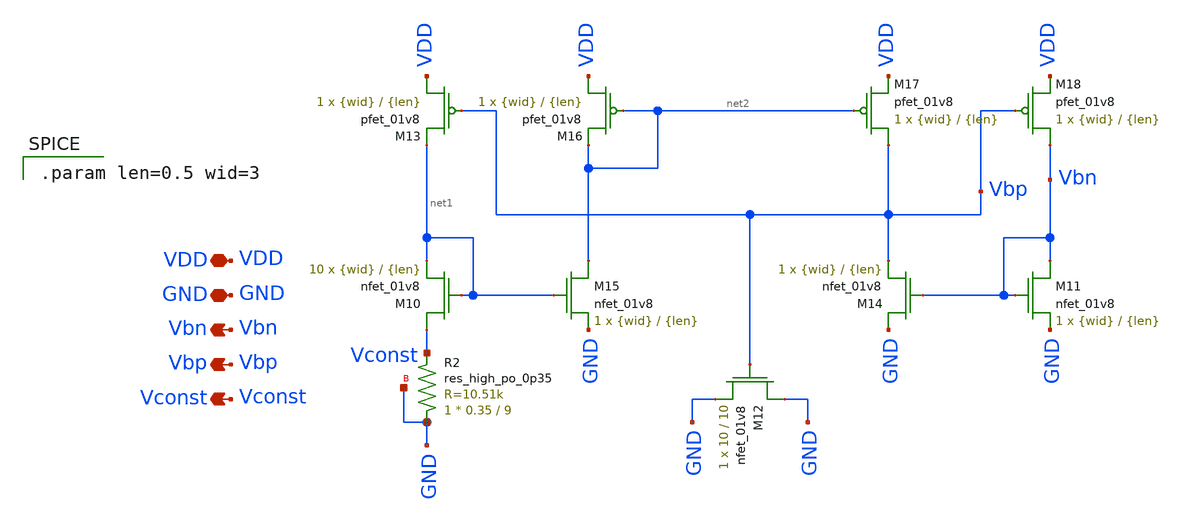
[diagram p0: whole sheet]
** sch_path: final/schematics/bias_gen/bias_gen.sch
**.subckt bias_gen VDD Vbp GND Vbn Vconst
*.iopin VDD
*.opin Vbp
*.iopin GND
*.opin Vbn
*.opin Vconst
XM10 Vconst net1 net1 GND sky130_fd_pr__nfet_01v8 L={len} W={wid} nf=1 ad='int((nf+1)/2) * W/nf * 0.29'
+ as='int((nf+2)/2) * W/nf * 0.29' pd='2*int((nf+1)/2) * (W/nf + 0.29)' ps='2*int((nf+2)/2) * (W/nf + 0.29)'
+ nrd='0.29 / W' nrs='0.29 / W' sa=0 sb=0 sd=0 mult=10 m=10
XM11 Vbn Vbn GND GND sky130_fd_pr__nfet_01v8 L={len} W={wid} nf=1 ad='int((nf+1)/2) * W/nf * 0.29' as='int((nf+2)/2) * W/nf * 0.29'
+ pd='2*int((nf+1)/2) * (W/nf + 0.29)' ps='2*int((nf+2)/2) * (W/nf + 0.29)' nrd='0.29 / W' nrs='0.29 / W'
+ sa=0 sb=0 sd=0 mult=1 m=1
XM12 GND Vbp GND GND sky130_fd_pr__nfet_01v8 L=10 W=10 nf=1 ad='int((nf+1)/2) * W/nf * 0.29' as='int((nf+2)/2) * W/nf * 0.29'
+ pd='2*int((nf+1)/2) * (W/nf + 0.29)' ps='2*int((nf+2)/2) * (W/nf + 0.29)' nrd='0.29 / W' nrs='0.29 / W'
+ sa=0 sb=0 sd=0 mult=1 m=1
XM13 VDD Vbp net1 VDD sky130_fd_pr__pfet_01v8 L={len} W={wid} nf=1 ad='int((nf+1)/2) * W/nf * 0.29' as='int((nf+2)/2) * W/nf * 0.29'
+ pd='2*int((nf+1)/2) * (W/nf + 0.29)' ps='2*int((nf+2)/2) * (W/nf + 0.29)' nrd='0.29 / W' nrs='0.29 / W'
+ sa=0 sb=0 sd=0 mult=1 m=1
XM14 GND Vbn Vbp GND sky130_fd_pr__nfet_01v8 L={len} W={wid} nf=1 ad='int((nf+1)/2) * W/nf * 0.29' as='int((nf+2)/2) * W/nf * 0.29'
+ pd='2*int((nf+1)/2) * (W/nf + 0.29)' ps='2*int((nf+2)/2) * (W/nf + 0.29)' nrd='0.29 / W' nrs='0.29 / W'
+ sa=0 sb=0 sd=0 mult=1 m=1
XM15 net2 net1 GND GND sky130_fd_pr__nfet_01v8 L={len} W={wid} nf=1 ad='int((nf+1)/2) * W/nf * 0.29'
+ as='int((nf+2)/2) * W/nf * 0.29' pd='2*int((nf+1)/2) * (W/nf + 0.29)' ps='2*int((nf+2)/2) * (W/nf + 0.29)'
+ nrd='0.29 / W' nrs='0.29 / W' sa=0 sb=0 sd=0 mult=1 m=1
XM16 VDD net2 net2 VDD sky130_fd_pr__pfet_01v8 L={len} W={wid} nf=1 ad='int((nf+1)/2) * W/nf * 0.29'
+ as='int((nf+2)/2) * W/nf * 0.29' pd='2*int((nf+1)/2) * (W/nf + 0.29)' ps='2*int((nf+2)/2) * (W/nf + 0.29)'
+ nrd='0.29 / W' nrs='0.29 / W' sa=0 sb=0 sd=0 mult=1 m=1
XM17 Vbp net2 VDD VDD sky130_fd_pr__pfet_01v8 L={len} W={wid} nf=1 ad='int((nf+1)/2) * W/nf * 0.29' as='int((nf+2)/2) * W/nf * 0.29'
+ pd='2*int((nf+1)/2) * (W/nf + 0.29)' ps='2*int((nf+2)/2) * (W/nf + 0.29)' nrd='0.29 / W' nrs='0.29 / W'
+ sa=0 sb=0 sd=0 mult=1 m=1
XM18 Vbn Vbp VDD VDD sky130_fd_pr__pfet_01v8 L={len} W={wid} nf=1 ad='int((nf+1)/2) * W/nf * 0.29' as='int((nf+2)/2) * W/nf * 0.29'
+ pd='2*int((nf+1)/2) * (W/nf + 0.29)' ps='2*int((nf+2)/2) * (W/nf + 0.29)' nrd='0.29 / W' nrs='0.29 / W'
+ sa=0 sb=0 sd=0 mult=1 m=1
XR2 GND Vconst GND sky130_fd_pr__res_high_po_0p35 L=9 mult=1 m=1
**** begin user architecture code

.param len=0.5 wid=3

**** end user architecture code
**.ends
.end
